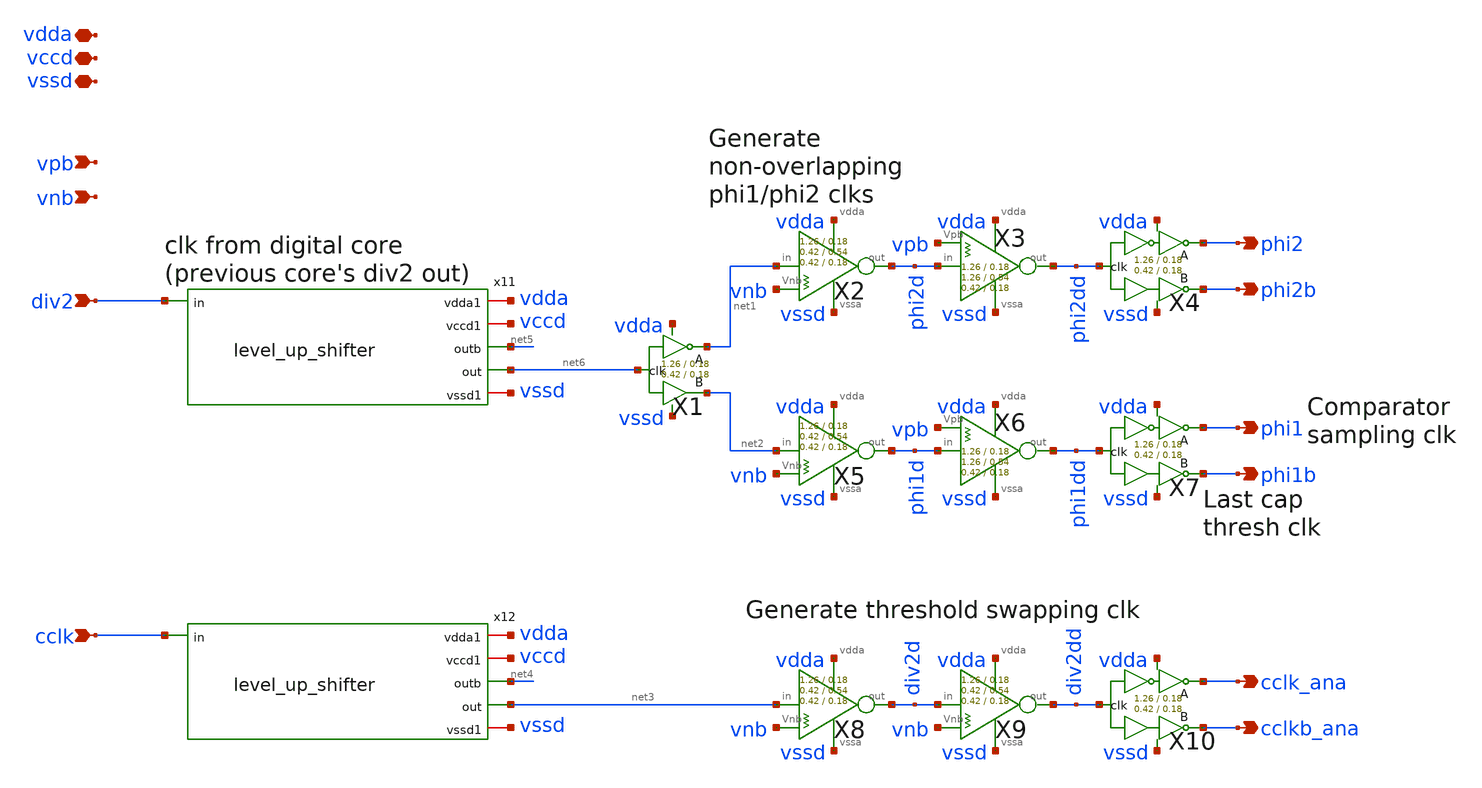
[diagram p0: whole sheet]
** sch_path: xschem/clkgen/filter_clkgen.sch
**.subckt filter_clkgen div2 phi2 phi2b phi1 phi1b cclk_ana cclkb_ana vpb vnb cclk vdda vccd vssd
*.ipin div2
*.opin phi2
*.opin phi2b
*.opin phi1
*.opin phi1b
*.opin cclk_ana
*.opin cclkb_ana
*.ipin vpb
*.ipin vnb
*.ipin cclk
*.iopin vdda
*.iopin vccd
*.iopin vssd
X4 phi2dd phi2 phi2b vdda vssd comp_clks Wpmos=1.26 Lpmos=0.18 Wnmos=0.42 Lnmos=0.18
X7 phi1dd phi1 phi1b vdda vssd comp_clks Wpmos=1.26 Lpmos=0.18 Wnmos=0.42 Lnmos=0.18
X10 div2dd cclk_ana cclkb_ana vdda vssd comp_clks Wpmos=1.26 Lpmos=0.18 Wnmos=0.42 Lnmos=0.18
X1 net6 net1 net2 vdda vssd comp_clks_1stage Wpmos=1.26 Lpmos=0.18 Wnmos=0.42 Lnmos=0.18
X2 net1 phi2d vnb vdda vssd inv_weak_pulldown Wpmos=1.26 Lpmos= Wnmos= Lnmos=0.54
X5 net2 phi1d vnb vdda vssd inv_weak_pulldown Wpmos=1.26 Lpmos= Wnmos= Lnmos=0.54
X8 net3 div2d vnb vdda vssd inv_weak_pulldown Wpmos=1.26 Lpmos= Wnmos= Lnmos=0.54
X9 div2d div2dd vnb vdda vssd inv_weak_pulldown Wpmos=1.26 Lpmos= Wnmos= Lnmos=0.54
X3 phi2d phi2dd vpb vdda vssd inv_weak_pullup Wpmos=1.26 Lpmos=0.54 Wnmos= Lnmos=
X6 phi1d phi1dd vpb vdda vssd inv_weak_pullup Wpmos=1.26 Lpmos=0.54 Wnmos= Lnmos=
x12 vdda vccd cclk net4 net3 vssd level_up_shifter
x11 vdda vccd div2 net5 net6 vssd level_up_shifter
**.ends
.end
